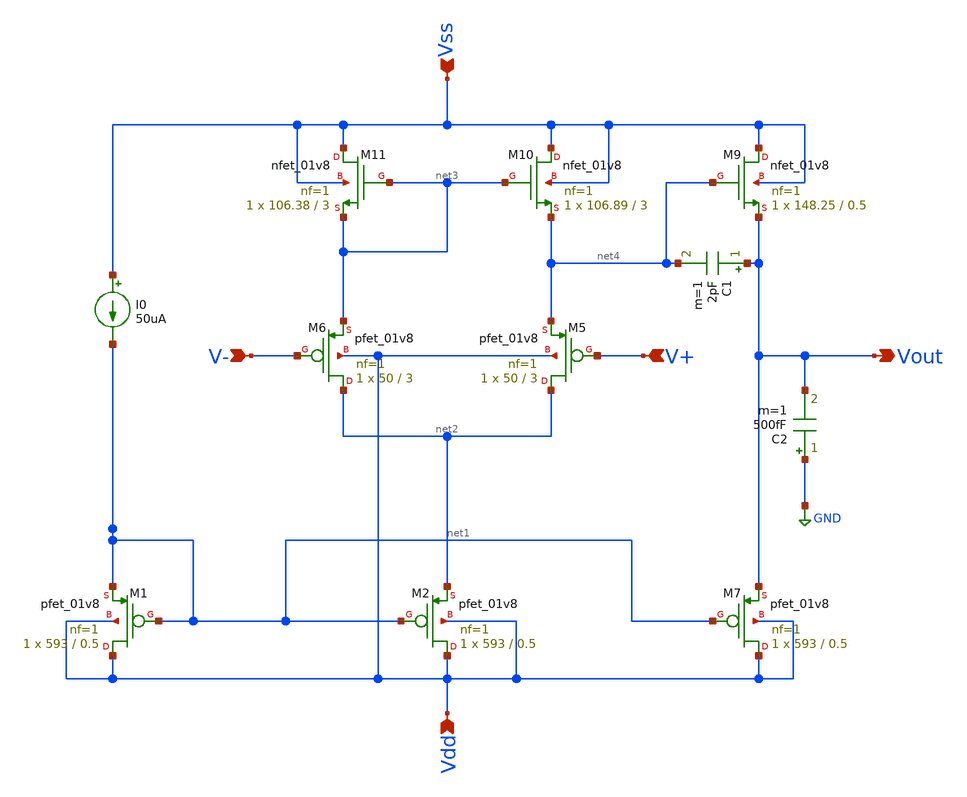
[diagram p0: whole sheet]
** sch_path: xschem/untitled-4.sch
**.subckt untitled-4 Vout Vdd Vss V+ V-
*.opin Vout
*.ipin Vdd
*.ipin Vss
*.ipin V+
*.ipin V-
XM10 Vss net3 net4 Vss sky130_fd_pr__nfet_01v8 L=3 W=106.89 nf=1 ad='int((1 + 1)/2) * 106.89 / 1 * 0.29'
+ as='int((1 + 2)/2) * 106.89 / 1 * 0.29' pd='2*int((1 + 1)/2) * (106.89 / 1 + 0.29)' ps='2*int((1 + 2)/2) * (106.89 / 1 + 0.29)'
+ nrd='0.29 / 106.89 ' nrs='0.29 / 106.89 ' sa=0 sb=0 sd=0 mult=1 m=1
XM11 Vss net3 net3 Vss sky130_fd_pr__nfet_01v8 L=3 W=106.38 nf=1 ad='int((1 + 1)/2) * 106.38 / 1 * 0.29'
+ as='int((1 + 2)/2) * 106.38 / 1 * 0.29' pd='2*int((1 + 1)/2) * (106.38 / 1 + 0.29)' ps='2*int((1 + 2)/2) * (106.38 / 1 + 0.29)'
+ nrd='0.29 / 106.38 ' nrs='0.29 / 106.38 ' sa=0 sb=0 sd=0 mult=1 m=1
XM5 net2 V+ net4 Vdd sky130_fd_pr__pfet_01v8 L=3 W=50 nf=1 ad='int((1 + 1)/2) * 50 / 1 * 0.29' as='int((1 + 2)/2) * 50 / 1 * 0.29'
+ pd='2*int((1 + 1)/2) * (50 / 1 + 0.29)' ps='2*int((1 + 2)/2) * (50 / 1 + 0.29)' nrd='0.29 / 50 ' nrs='0.29 / 50 '
+ sa=0 sb=0 sd=0 mult=1 m=1
XM6 net2 V- net3 Vdd sky130_fd_pr__pfet_01v8 L=3 W=50 nf=1 ad='int((1 + 1)/2) * 50 / 1 * 0.29' as='int((1 + 2)/2) * 50 / 1 * 0.29'
+ pd='2*int((1 + 1)/2) * (50 / 1 + 0.29)' ps='2*int((1 + 2)/2) * (50 / 1 + 0.29)' nrd='0.29 / 50 ' nrs='0.29 / 50 '
+ sa=0 sb=0 sd=0 mult=1 m=1
C1 Vout net4 2pF m=1
C2 GND Vout 500fF m=1
XM7 Vdd net1 Vout Vdd sky130_fd_pr__pfet_01v8 L=0.5 W=593 nf=1 ad='int((1 + 1)/2) * 593 / 1 * 0.29' as='int((1 + 2)/2) * 593 / 1 * 0.29'
+ pd='2*int((1 + 1)/2) * (593 / 1 + 0.29)' ps='2*int((1 + 2)/2) * (593 / 1 + 0.29)' nrd='0.29 / 593 ' nrs='0.29 / 593 '
+ sa=0 sb=0 sd=0 mult=1 m=1
XM9 Vss net4 Vout Vss sky130_fd_pr__nfet_01v8 L=0.5 W=148.25 nf=1 ad='int((1 + 1)/2) * 148.25 / 1 * 0.29'
+ as='int((1 + 2)/2) * 148.25 / 1 * 0.29' pd='2*int((1 + 1)/2) * (148.25 / 1 + 0.29)' ps='2*int((1 + 2)/2) * (148.25 / 1 + 0.29)'
+ nrd='0.29 / 148.25 ' nrs='0.29 / 148.25 ' sa=0 sb=0 sd=0 mult=1 m=1
I0 Vss net1 50uA
XM2 Vdd net1 net2 Vdd sky130_fd_pr__pfet_01v8 L=0.5 W=593 nf=1 ad='int((1 + 1)/2) * 593 / 1 * 0.29' as='int((1 + 2)/2) * 593 / 1 * 0.29'
+ pd='2*int((1 + 1)/2) * (593 / 1 + 0.29)' ps='2*int((1 + 2)/2) * (593 / 1 + 0.29)' nrd='0.29 / 593 ' nrs='0.29 / 593 '
+ sa=0 sb=0 sd=0 mult=1 m=1
XM1 Vdd net1 net1 Vdd sky130_fd_pr__pfet_01v8 L=0.5 W=593 nf=1 ad='int((1 + 1)/2) * 593 / 1 * 0.29' as='int((1 + 2)/2) * 593 / 1 * 0.29'
+ pd='2*int((1 + 1)/2) * (593 / 1 + 0.29)' ps='2*int((1 + 2)/2) * (593 / 1 + 0.29)' nrd='0.29 / 593 ' nrs='0.29 / 593 '
+ sa=0 sb=0 sd=0 mult=1 m=1
**.ends
.GLOBAL GND
.end
